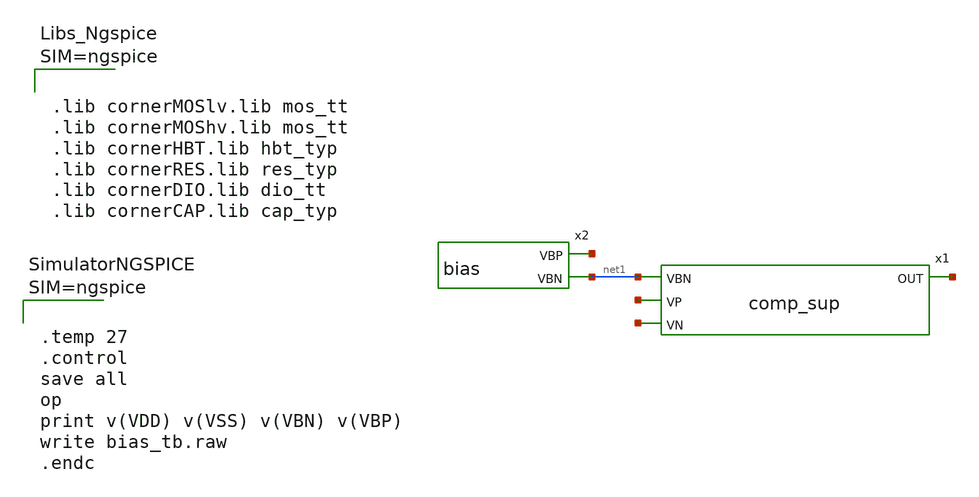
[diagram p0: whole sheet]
** sch_path: design/blocks/bias/schematic/untitled.sch
**.subckt untitled
x1 net1 net2 net3 net4 VDD VSS comp_sup
x2 net5 net1 VDD VSS bias
**** begin user architecture code



.lib cornerMOSlv.lib mos_tt
.lib cornerMOShv.lib mos_tt
.lib cornerHBT.lib hbt_typ
.lib cornerRES.lib res_typ
.lib cornerDIO.lib dio_tt
.lib cornerCAP.lib cap_typ






.temp 27
.control
save all
op
print v(VDD) v(VSS) v(VBN) v(VBP)
write bias_tb.raw
.endc



**** end user architecture code
**.ends

* expanding   symbol:  comp_sup.sym # of pins=4
** sym_path: design/blocks/comparator/schematic/comp_sup.sym
** sch_path: design/blocks/comparator/schematic/comp_sup.sch
.subckt comp_sup VBN VP VN OUT VDD VSS
*.opin OUT
*.ipin VN
*.ipin VP
*.ipin VBN
XM2 DIO DIO VDD VDD sg13_lv_pmos w=2u l=4u ng=1 m=1 mm_ok=1
XM3 OUT1 DIO VDD VDD sg13_lv_pmos w=2u l=4u ng=1 m=1 mm_ok=1
XM4 DIO VP TAIL VSS sg13_lv_nmos w=20u l=2u ng=4 m=1 mm_ok=1
XM5 OUT1 VN TAIL VSS sg13_lv_nmos w=20u l=2u ng=4 m=1 mm_ok=1
XM6 TAIL VBN VSS VSS sg13_lv_nmos w=2u l=4u ng=1 m=1 mm_ok=1
XM1 OUT2 OUT1 VDD VDD sg13_lv_pmos w=4u l=4u ng=1 m=1 mm_ok=1
XM7 OUT2 VBN VSS VSS sg13_lv_nmos w=2u l=4u ng=1 m=1 mm_ok=1
x1 OUT2 OUT VDD VSS schmitt
.ends


* expanding   symbol:  bias.sym # of pins=2
** sym_path: design/blocks/bias/schematic/bias.sym
** sch_path: design/blocks/bias/schematic/bias.sch
.subckt bias VBP VBN VDD VSS
*.opin VBP
*.opin VBN
XM1 VBN VBN VSS VSS sg13_lv_nmos w=2u l=1u ng=1 m=1 mm_ok=1
XM2 VBP VBP VDD VDD sg13_lv_pmos w=2u l=1u ng=1 m=1 mm_ok=1
XR2 VBP VSS VSS rhigh w=0.5e-6 l=10.0e-6 m=1 b=0 mm_ok=1
XR1 VDD VBN VSS rhigh w=0.5e-6 l=10.0e-6 m=1 b=0 mm_ok=1
XC1 VBN VSS cap_cmim w=26.0e-6 l=26.0e-6 m=1 mm_ok=1
XC2 VDD VBP cap_cmim w=26.0e-6 l=26.0e-6 m=1 mm_ok=1
.ends


* expanding   symbol:  schmitt.sym # of pins=2
** sym_path: design/blocks/schmitt/schematic/schmitt.sym
** sch_path: design/blocks/schmitt/schematic/schmitt.sch
.subckt schmitt IN OUT VDD VSS
*.opin OUT
*.ipin IN
XM4 net1 IN VDD VDD sg13_lv_pmos w=1.04u l=0.13u ng=1 m=1 mm_ok=1
XM6 OUT IN net2 VSS sg13_lv_nmos w=0.76u l=0.13u ng=1 m=1 mm_ok=1
XM5 OUT IN net1 VDD sg13_lv_pmos w=1.04u l=0.13u ng=1 m=1 mm_ok=1
XM7 net2 IN VSS VSS sg13_lv_nmos w=0.76u l=0.13u ng=1 m=1 mm_ok=1
XM8 VSS OUT net1 VDD sg13_lv_pmos w=0.42u l=0.13u ng=1 m=1 mm_ok=1
XM9 VDD OUT net2 VSS sg13_lv_nmos w=0.42u l=0.13u ng=1 m=1 mm_ok=1
.ends

.end
